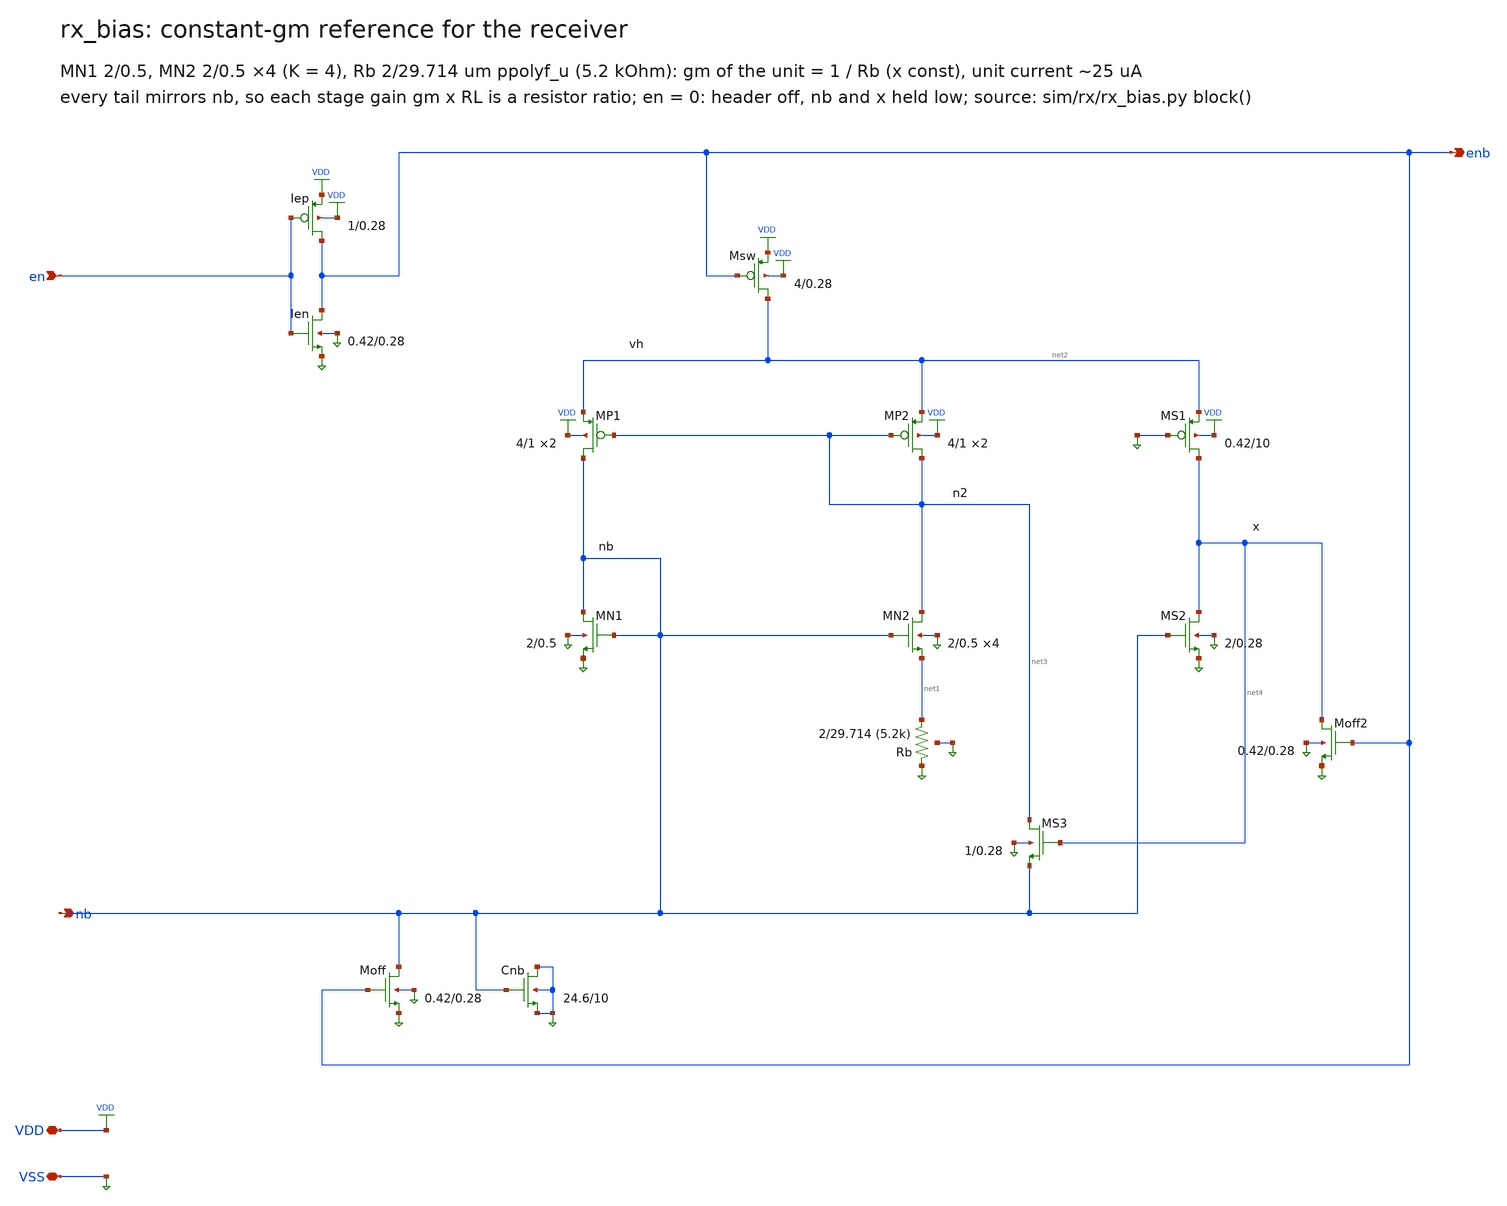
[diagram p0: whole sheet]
** sch_path: xschem/rx_bias.sch
**.subckt rx_bias VDD VSS en enb nb
*.iopin VDD
*.iopin VSS
*.ipin en
*.opin enb
*.opin nb
XMsw net2 enb VDD VDD pfet_03v3 L=0.28u W=4.0u nf=1 ad=2.0p as=2.0p pd=9.0u ps=9.0u nrd=0 nrs=0 sa=0
+ sb=0 sd=0 m=1
XMP1 nb net3 net2 VDD pfet_03v3 L=1.0u W=4.0u nf=1 ad=2.0p as=2.0p pd=9.0u ps=9.0u nrd=0 nrs=0 sa=0
+ sb=0 sd=0 m=2
XMP2 net3 net3 net2 VDD pfet_03v3 L=1.0u W=4.0u nf=1 ad=2.0p as=2.0p pd=9.0u ps=9.0u nrd=0 nrs=0
+ sa=0 sb=0 sd=0 m=2
XMN1 nb nb VSS VSS nfet_03v3 L=0.5u W=2.0u nf=1 ad=1.0p as=1.0p pd=5.0u ps=5.0u nrd=0 nrs=0 sa=0
+ sb=0 sd=0 m=1
XMN2 net3 nb net1 VSS nfet_03v3 L=0.5u W=2.0u nf=1 ad=1.0p as=1.0p pd=5.0u ps=5.0u nrd=0 nrs=0 sa=0
+ sb=0 sd=0 m=4
XMS1 net4 VSS net2 VDD pfet_03v3 L=10.0u W=0.41999999999999993u nf=1 ad=0.20999999999999996p
+ as=0.20999999999999996p pd=1.8399999999999999u ps=1.8399999999999999u nrd=0 nrs=0 sa=0 sb=0 sd=0 m=1
XMS2 net4 nb VSS VSS nfet_03v3 L=0.28u W=2.0u nf=1 ad=1.0p as=1.0p pd=5.0u ps=5.0u nrd=0 nrs=0 sa=0
+ sb=0 sd=0 m=1
XMS3 net3 net4 nb VSS nfet_03v3 L=0.28u W=1.0u nf=1 ad=0.5p as=0.5p pd=3.0u ps=3.0u nrd=0 nrs=0 sa=0
+ sb=0 sd=0 m=1
XMoff nb enb VSS VSS nfet_03v3 L=0.28u W=0.41999999999999993u nf=1 ad=0.20999999999999996p
+ as=0.20999999999999996p pd=1.8399999999999999u ps=1.8399999999999999u nrd=0 nrs=0 sa=0 sb=0 sd=0 m=1
XMoff2 net4 enb VSS VSS nfet_03v3 L=0.28u W=0.41999999999999993u nf=1 ad=0.20999999999999996p
+ as=0.20999999999999996p pd=1.8399999999999999u ps=1.8399999999999999u nrd=0 nrs=0 sa=0 sb=0 sd=0 m=1
XRb net1 VSS VSS ppolyf_u r_width=2.0e-6 r_length=29.714000000000002e-6 m=1
XCnb VSS nb VSS VSS nfet_03v3 L=10.0u W=24.57u nf=1 ad=12.285p as=12.285p pd=50.14u ps=50.14u nrd=0
+ nrs=0 sa=0 sb=0 sd=0 m=1
XIep enb en VDD VDD pfet_03v3 L=0.28u W=1.0u nf=1 ad=0.5p as=0.5p pd=3.0u ps=3.0u nrd=0 nrs=0 sa=0
+ sb=0 sd=0 m=1
XIen enb en VSS VSS nfet_03v3 L=0.28u W=0.41999999999999993u nf=1 ad=0.20999999999999996p
+ as=0.20999999999999996p pd=1.8399999999999999u ps=1.8399999999999999u nrd=0 nrs=0 sa=0 sb=0 sd=0 m=1
**.ends
.end
